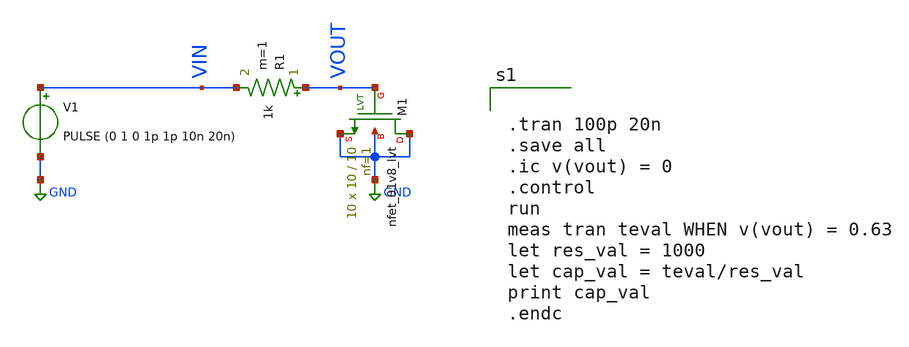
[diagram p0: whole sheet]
** sch_path: cgate-ext_circuit_LASCAS2024.sch
**.subckt cgate-ext_circuit_LASCAS2024
R1 VOUT VIN 1k m=1
V1 VIN GND PULSE (0 1 0 1p 1p 10n 20n)
XM1 GND VOUT GND GND sky130_fd_pr__nfet_01v8_lvt L=10 W=10 nf=1 ad='int((nf+1)/2) * W/nf * 0.29' as='int((nf+2)/2) * W/nf * 0.29'
+ pd='2*int((nf+1)/2) * (W/nf + 0.29)' ps='2*int((nf+2)/2) * (W/nf + 0.29)' nrd='0.29 / W' nrs='0.29 / W'
+ sa=0 sb=0 sd=0 mult=10 m=10
**** begin user architecture code


.tran 100p 20n
.save all
.ic v(vout) = 0
.control
run
meas tran teval WHEN v(vout) = 0.63
let res_val = 1000
let cap_val = teval/res_val
print cap_val
.endc



** opencircuitdesign pdks install
.lib $::SKYWATER_MODELS/sky130.lib.spice tt


**** end user architecture code
**.ends
.GLOBAL GND
.end
